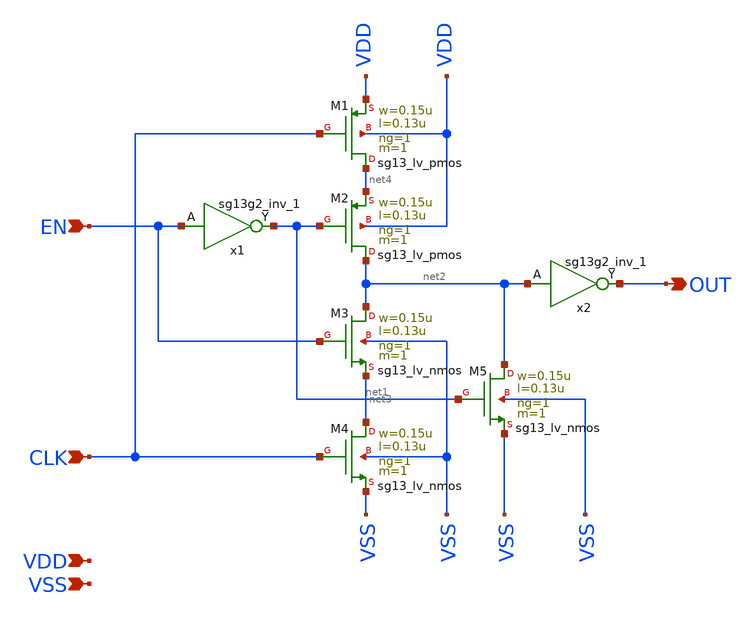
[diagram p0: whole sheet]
** sch_path: designs/sampling_driver/sampling_driver.sch
**.subckt sampling_driver CLK EN OUT VDD VSS
*.ipin CLK
*.ipin EN
*.opin OUT
*.ipin VDD
*.ipin VSS
XM1 net4 CLK VDD VDD sg13_lv_pmos w=0.15u l=0.13u ng=1 m=1 mm_ok=1
XM2 net2 net1 net4 VDD sg13_lv_pmos w=0.15u l=0.13u ng=1 m=1 mm_ok=1
XM3 net2 EN net3 VSS sg13_lv_nmos w=0.15u l=0.13u ng=1 m=1 mm_ok=1
XM4 net3 CLK VSS VSS sg13_lv_nmos w=0.15u l=0.13u ng=1 m=1 mm_ok=1
x1 net1 EN VDD VSS sg13g2_inv_1
XM5 net2 net1 VSS VSS sg13_lv_nmos w=0.15u l=0.13u ng=1 m=1 mm_ok=1
x2 OUT net2 VDD VSS sg13g2_inv_1
**.ends

* expanding   symbol:  sg13g2_stdcells/sg13g2_inv_1.sym # of pins=2
** sym_path: sg13g2_stdcells/sg13g2_inv_1.sym
** sch_path: sg13g2_stdcells/sg13g2_inv_1.sch
.subckt sg13g2_inv_1 Y A VDD VSS
*.opin Y
*.ipin A
*.iopin VDD
*.iopin VSS
XM1 Y A VSS VSS sg13_lv_nmos w=740.00n l=130.00n ng=1 m=1 mm_ok=1
XM2 Y A VDD VDD sg13_lv_pmos w=1.12u l=130.00n ng=1 m=1 mm_ok=1
.ends

.end
